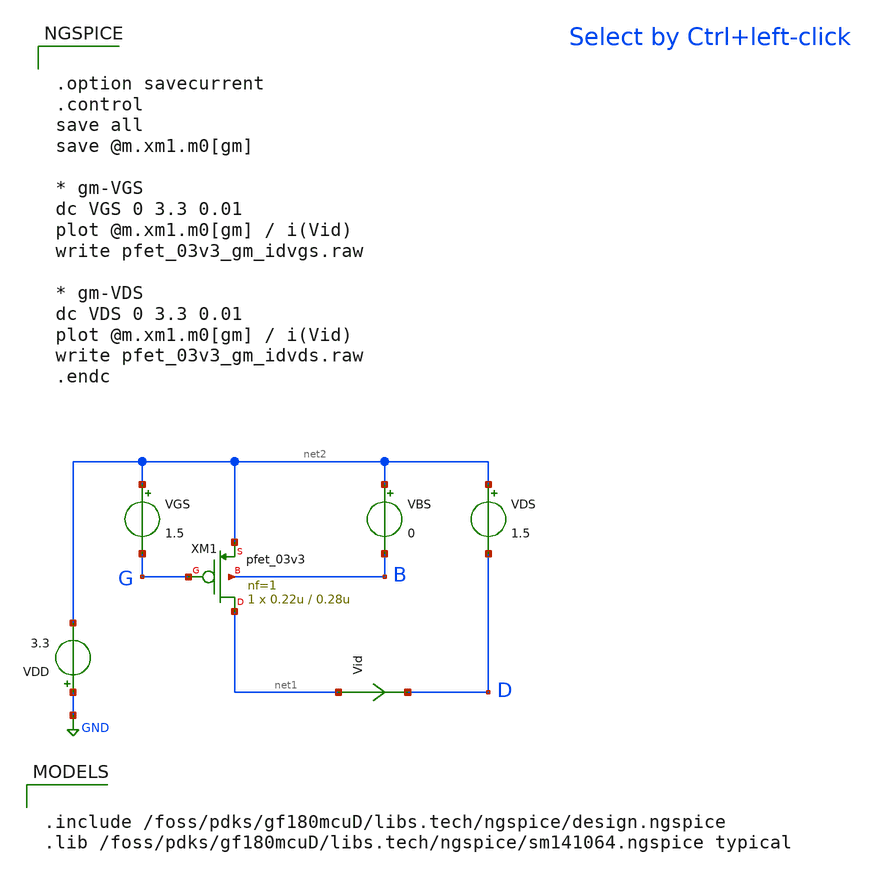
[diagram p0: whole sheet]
** sch_path: mosfet_gf180/pfet_03v3_gm.sch
**.subckt pfet_03v3_gm
VBS net2 B 0
VGS net2 G 1.5
VDS net2 D 1.5
Vid net1 D 0
.save i(vid)
XM1 net1 G net2 B pfet_03v3 L=0.28u W=0.22u nf=1 ad='int((nf+1)/2) * W/nf * 0.18u' as='int((nf+2)/2) * W/nf * 0.18u'
+ pd='2*int((nf+1)/2) * (W/nf + 0.18u)' ps='2*int((nf+2)/2) * (W/nf + 0.18u)' nrd='0.18u / W' nrs='0.18u / W'
+ sa=0 sb=0 sd=0 m=1
VDD GND net2 3.3
**** begin user architecture code

.include /foss/pdks/gf180mcuD/libs.tech/ngspice/design.ngspice
.lib /foss/pdks/gf180mcuD/libs.tech/ngspice/sm141064.ngspice typical



.option savecurrent
.control
save all
save @m.xm1.m0[gm]

* gm-VGS
dc VGS 0 3.3 0.01
plot @m.xm1.m0[gm] / i(Vid)
write pfet_03v3_gm_idvgs.raw

* gm-VDS
dc VDS 0 3.3 0.01
plot @m.xm1.m0[gm] / i(Vid)
write pfet_03v3_gm_idvds.raw
.endc


**** end user architecture code
**.ends
.GLOBAL GND
.end
